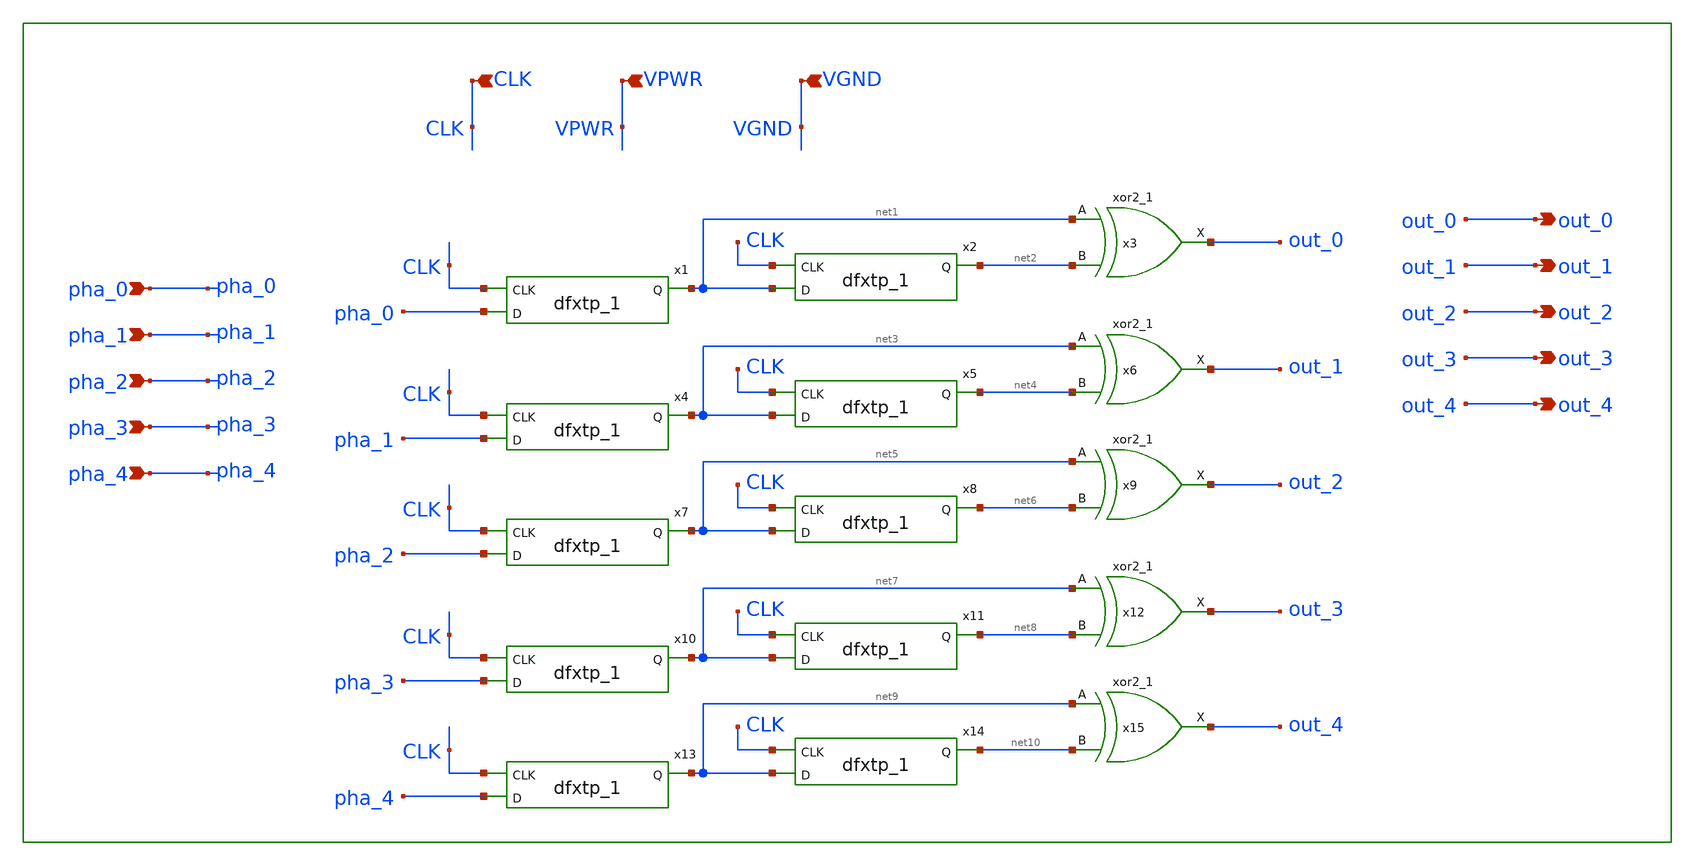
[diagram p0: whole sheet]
** sch_path: circuit/library/quantizer.sch
**.subckt quantizer CLK VPWR pha_0 pha_1 pha_2 pha_3 pha_4 out_0 out_1 out_2 out_3 out_4 VGND
*.ipin CLK
*.ipin VPWR
*.ipin pha_0
*.ipin pha_1
*.ipin pha_2
*.ipin pha_3
*.ipin pha_4
*.opin out_0
*.opin out_1
*.opin out_2
*.opin out_3
*.opin out_4
*.ipin VGND
x1 CLK pha_0 VGND VGND VPWR VPWR net1 sky130_fd_sc_hd__dfxtp_1
x2 CLK net1 VGND VGND VPB VPWR net2 sky130_fd_sc_hd__dfxtp_1
x3 net1 net2 VGND VGND VPWR VPWR out_0 sky130_fd_sc_hd__xor2_1
x4 CLK pha_1 VGND VGND VPWR VPWR net3 sky130_fd_sc_hd__dfxtp_1
x5 CLK net3 VGND VGND VPB VPWR net4 sky130_fd_sc_hd__dfxtp_1
x6 net3 net4 VGND VGND VPWR VPWR out_1 sky130_fd_sc_hd__xor2_1
x7 CLK pha_2 VGND VGND VPWR VPWR net5 sky130_fd_sc_hd__dfxtp_1
x8 CLK net5 VGND VGND VPB VPWR net6 sky130_fd_sc_hd__dfxtp_1
x9 net5 net6 VGND VGND VPWR VPWR out_2 sky130_fd_sc_hd__xor2_1
x10 CLK pha_3 VGND VGND VPWR VPWR net7 sky130_fd_sc_hd__dfxtp_1
x11 CLK net7 VGND VGND VPB VPWR net8 sky130_fd_sc_hd__dfxtp_1
x12 net7 net8 VGND VGND VPWR VPWR out_3 sky130_fd_sc_hd__xor2_1
x13 CLK pha_4 VGND VGND VPWR VPWR net9 sky130_fd_sc_hd__dfxtp_1
x14 CLK net9 VGND VGND VPB VPWR net10 sky130_fd_sc_hd__dfxtp_1
x15 net9 net10 VGND VGND VPWR VPWR out_4 sky130_fd_sc_hd__xor2_1
**.ends
.end
